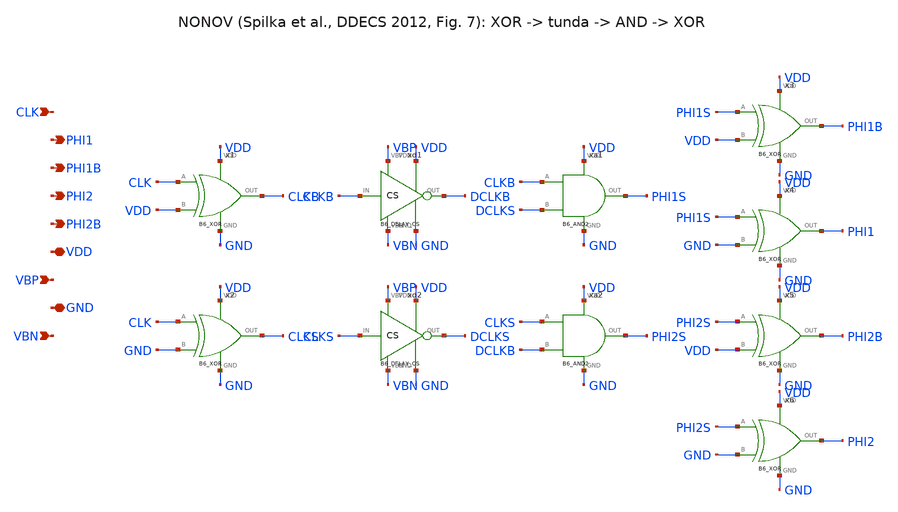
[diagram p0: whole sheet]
** sch_path: blocks/06_Clock_gen/xschem/B6_NONOV.sch
**.subckt B6_NONOV CLK PHI1 PHI1B PHI2 PHI2B VDD VBP GND VBN
*.ipin CLK
*.opin PHI1
*.opin PHI1B
*.opin PHI2
*.opin PHI2B
*.iopin VDD
*.ipin VBP
*.iopin GND
*.ipin VBN
x1 CLK VDD CLKB VDD GND B6_XOR
x2 CLK GND CLKS VDD GND B6_XOR
xd1 CLKB DCLKB VBP VDD VBN GND B6_DELAY_CS
xd2 CLKS DCLKS VBP VDD VBN GND B6_DELAY_CS
xa1 CLKB DCLKS PHI1S VDD GND B6_AND2
xa2 CLKS DCLKB PHI2S VDD GND B6_AND2
x3 PHI1S VDD PHI1B VDD GND B6_XOR
x4 PHI1S GND PHI1 VDD GND B6_XOR
x5 PHI2S VDD PHI2B VDD GND B6_XOR
x6 PHI2S GND PHI2 VDD GND B6_XOR
**.ends

* expanding   symbol:  blocks/06_Clock_gen/xschem/B6_XOR.sym # of pins=5
** sym_path: blocks/06_Clock_gen/xschem/B6_XOR.sym
** sch_path: blocks/06_Clock_gen/xschem/B6_XOR.sch
.subckt B6_XOR A B OUT VDD GND
*.ipin A
*.ipin B
*.opin OUT
*.iopin VDD
*.iopin GND
XMPA VDD A net1 VDD sky130_fd_pr__pfet_01v8 L=0.15 W=4 nf=1 ad='int((1 + 1)/2) * 4 / 1 * 0.29' as='int((1 + 2)/2) * 4 / 1 * 0.29'
+ pd='2*int((1 + 1)/2) * (4 / 1 + 0.29)' ps='2*int((1 + 2)/2) * (4 / 1 + 0.29)' nrd='0.29 / 4 ' nrs='0.29 / 4 '
+ sa=0 sb=0 sd=0 mult=1 m=1
XMPB VDD B net1 VDD sky130_fd_pr__pfet_01v8 L=0.15 W=4 nf=1 ad='int((1 + 1)/2) * 4 / 1 * 0.29' as='int((1 + 2)/2) * 4 / 1 * 0.29'
+ pd='2*int((1 + 1)/2) * (4 / 1 + 0.29)' ps='2*int((1 + 2)/2) * (4 / 1 + 0.29)' nrd='0.29 / 4 ' nrs='0.29 / 4 '
+ sa=0 sb=0 sd=0 mult=1 m=1
XMPC net1 C OUT VDD sky130_fd_pr__pfet_01v8 L=0.15 W=4 nf=1 ad='int((1 + 1)/2) * 4 / 1 * 0.29' as='int((1 + 2)/2) * 4 / 1 * 0.29'
+ pd='2*int((1 + 1)/2) * (4 / 1 + 0.29)' ps='2*int((1 + 2)/2) * (4 / 1 + 0.29)' nrd='0.29 / 4 ' nrs='0.29 / 4 '
+ sa=0 sb=0 sd=0 mult=1 m=1
XMNA OUT A net2 GND sky130_fd_pr__nfet_01v8 L=0.15 W=2 nf=1 ad='int((1 + 1)/2) * 2 / 1 * 0.29' as='int((1 + 2)/2) * 2 / 1 * 0.29'
+ pd='2*int((1 + 1)/2) * (2 / 1 + 0.29)' ps='2*int((1 + 2)/2) * (2 / 1 + 0.29)' nrd='0.29 / 2 ' nrs='0.29 / 2 '
+ sa=0 sb=0 sd=0 mult=1 m=1
XMNB net2 B GND GND sky130_fd_pr__nfet_01v8 L=0.15 W=2 nf=1 ad='int((1 + 1)/2) * 2 / 1 * 0.29' as='int((1 + 2)/2) * 2 / 1 * 0.29'
+ pd='2*int((1 + 1)/2) * (2 / 1 + 0.29)' ps='2*int((1 + 2)/2) * (2 / 1 + 0.29)' nrd='0.29 / 2 ' nrs='0.29 / 2 '
+ sa=0 sb=0 sd=0 mult=1 m=1
XMNC OUT C GND GND sky130_fd_pr__nfet_01v8 L=0.15 W=1 nf=1 ad='int((1 + 1)/2) * 1 / 1 * 0.29' as='int((1 + 2)/2) * 1 / 1 * 0.29'
+ pd='2*int((1 + 1)/2) * (1 / 1 + 0.29)' ps='2*int((1 + 2)/2) * (1 / 1 + 0.29)' nrd='0.29 / 1 ' nrs='0.29 / 1 '
+ sa=0 sb=0 sd=0 mult=1 m=1
xnor A B C VDD GND B6_NOR2
.ends


* expanding   symbol:  blocks/06_Clock_gen/xschem/B6_DELAY_CS.sym # of pins=6
** sym_path: blocks/06_Clock_gen/xschem/B6_DELAY_CS.sym
** sch_path: blocks/06_Clock_gen/xschem/B6_DELAY_CS.sch
.subckt B6_DELAY_CS IN OUT VBP VDD VBN GND
*.ipin IN
*.ipin VBP
*.iopin VDD
*.opin OUT
*.ipin VBN
*.iopin GND
XMPS VDD VBP net1 VDD sky130_fd_pr__pfet_01v8 L=1 W=1 nf=1 ad='int((1 + 1)/2) * 1 / 1 * 0.29' as='int((1 + 2)/2) * 1 / 1 * 0.29'
+ pd='2*int((1 + 1)/2) * (1 / 1 + 0.29)' ps='2*int((1 + 2)/2) * (1 / 1 + 0.29)' nrd='0.29 / 1 ' nrs='0.29 / 1 '
+ sa=0 sb=0 sd=0 mult=1 m=1
XMPI net1 IN OUT VDD sky130_fd_pr__pfet_01v8 L=0.15 W=1 nf=1 ad='int((1 + 1)/2) * 1 / 1 * 0.29' as='int((1 + 2)/2) * 1 / 1 * 0.29'
+ pd='2*int((1 + 1)/2) * (1 / 1 + 0.29)' ps='2*int((1 + 2)/2) * (1 / 1 + 0.29)' nrd='0.29 / 1 ' nrs='0.29 / 1 '
+ sa=0 sb=0 sd=0 mult=1 m=1
XMNI OUT IN net2 GND sky130_fd_pr__nfet_01v8 L=0.15 W=0.5 nf=1 ad='int((1 + 1)/2) * 0.5 / 1 * 0.29' as='int((1 + 2)/2) * 0.5 / 1 * 0.29'
+ pd='2*int((1 + 1)/2) * (0.5 / 1 + 0.29)' ps='2*int((1 + 2)/2) * (0.5 / 1 + 0.29)' nrd='0.29 / 0.5 ' nrs='0.29 / 0.5 '
+ sa=0 sb=0 sd=0 mult=1 m=1
XMNS net2 VBN GND GND sky130_fd_pr__nfet_01v8 L=1 W=0.5 nf=1 ad='int((1 + 1)/2) * 0.5 / 1 * 0.29' as='int((1 + 2)/2) * 0.5 / 1 * 0.29'
+ pd='2*int((1 + 1)/2) * (0.5 / 1 + 0.29)' ps='2*int((1 + 2)/2) * (0.5 / 1 + 0.29)' nrd='0.29 / 0.5 ' nrs='0.29 / 0.5 '
+ sa=0 sb=0 sd=0 mult=1 m=1
XC1 OUT GND sky130_fd_pr__cap_mim_m3_1 W=1 L=1 MF=4 m=4
.ends


* expanding   symbol:  blocks/06_Clock_gen/xschem/B6_AND2.sym # of pins=5
** sym_path: blocks/06_Clock_gen/xschem/B6_AND2.sym
** sch_path: blocks/06_Clock_gen/xschem/B6_AND2.sch
.subckt B6_AND2 A B OUT VDD GND
*.ipin A
*.ipin B
*.opin OUT
*.iopin VDD
*.iopin GND
xnand A B net1 VDD GND B6_NAND2
xinv net1 OUT VDD GND B6_INV
.ends


* expanding   symbol:  blocks/06_Clock_gen/xschem/B6_NOR2.sym # of pins=5
** sym_path: blocks/06_Clock_gen/xschem/B6_NOR2.sym
** sch_path: blocks/06_Clock_gen/xschem/B6_NOR2.sch
.subckt B6_NOR2 A B OUT VDD GND
*.ipin A
*.ipin B
*.opin OUT
*.iopin VDD
*.iopin GND
XMPA VDD A net1 VDD sky130_fd_pr__pfet_01v8 L=0.15 W=4 nf=1 ad='int((1 + 1)/2) * 4 / 1 * 0.29' as='int((1 + 2)/2) * 4 / 1 * 0.29'
+ pd='2*int((1 + 1)/2) * (4 / 1 + 0.29)' ps='2*int((1 + 2)/2) * (4 / 1 + 0.29)' nrd='0.29 / 4 ' nrs='0.29 / 4 '
+ sa=0 sb=0 sd=0 mult=1 m=1
XMPB net1 B OUT VDD sky130_fd_pr__pfet_01v8 L=0.15 W=4 nf=1 ad='int((1 + 1)/2) * 4 / 1 * 0.29' as='int((1 + 2)/2) * 4 / 1 * 0.29'
+ pd='2*int((1 + 1)/2) * (4 / 1 + 0.29)' ps='2*int((1 + 2)/2) * (4 / 1 + 0.29)' nrd='0.29 / 4 ' nrs='0.29 / 4 '
+ sa=0 sb=0 sd=0 mult=1 m=1
XMNA OUT A GND GND sky130_fd_pr__nfet_01v8 L=0.15 W=1 nf=1 ad='int((1 + 1)/2) * 1 / 1 * 0.29' as='int((1 + 2)/2) * 1 / 1 * 0.29'
+ pd='2*int((1 + 1)/2) * (1 / 1 + 0.29)' ps='2*int((1 + 2)/2) * (1 / 1 + 0.29)' nrd='0.29 / 1 ' nrs='0.29 / 1 '
+ sa=0 sb=0 sd=0 mult=1 m=1
XMNB OUT B GND GND sky130_fd_pr__nfet_01v8 L=0.15 W=1 nf=1 ad='int((1 + 1)/2) * 1 / 1 * 0.29' as='int((1 + 2)/2) * 1 / 1 * 0.29'
+ pd='2*int((1 + 1)/2) * (1 / 1 + 0.29)' ps='2*int((1 + 2)/2) * (1 / 1 + 0.29)' nrd='0.29 / 1 ' nrs='0.29 / 1 '
+ sa=0 sb=0 sd=0 mult=1 m=1
.ends


* expanding   symbol:  blocks/06_Clock_gen/xschem/B6_NAND2.sym # of pins=5
** sym_path: blocks/06_Clock_gen/xschem/B6_NAND2.sym
** sch_path: blocks/06_Clock_gen/xschem/B6_NAND2.sch
.subckt B6_NAND2 A B OUT VDD GND
*.ipin A
*.ipin B
*.opin OUT
*.iopin VDD
*.iopin GND
XMPA VDD A OUT VDD sky130_fd_pr__pfet_01v8 L=0.15 W=2 nf=1 ad='int((1 + 1)/2) * 2 / 1 * 0.29' as='int((1 + 2)/2) * 2 / 1 * 0.29'
+ pd='2*int((1 + 1)/2) * (2 / 1 + 0.29)' ps='2*int((1 + 2)/2) * (2 / 1 + 0.29)' nrd='0.29 / 2 ' nrs='0.29 / 2 '
+ sa=0 sb=0 sd=0 mult=1 m=1
XMPB VDD B OUT VDD sky130_fd_pr__pfet_01v8 L=0.15 W=2 nf=1 ad='int((1 + 1)/2) * 2 / 1 * 0.29' as='int((1 + 2)/2) * 2 / 1 * 0.29'
+ pd='2*int((1 + 1)/2) * (2 / 1 + 0.29)' ps='2*int((1 + 2)/2) * (2 / 1 + 0.29)' nrd='0.29 / 2 ' nrs='0.29 / 2 '
+ sa=0 sb=0 sd=0 mult=1 m=1
XMNA OUT A net1 GND sky130_fd_pr__nfet_01v8 L=0.15 W=2 nf=1 ad='int((1 + 1)/2) * 2 / 1 * 0.29' as='int((1 + 2)/2) * 2 / 1 * 0.29'
+ pd='2*int((1 + 1)/2) * (2 / 1 + 0.29)' ps='2*int((1 + 2)/2) * (2 / 1 + 0.29)' nrd='0.29 / 2 ' nrs='0.29 / 2 '
+ sa=0 sb=0 sd=0 mult=1 m=1
XMNB net1 B GND GND sky130_fd_pr__nfet_01v8 L=0.15 W=2 nf=1 ad='int((1 + 1)/2) * 2 / 1 * 0.29' as='int((1 + 2)/2) * 2 / 1 * 0.29'
+ pd='2*int((1 + 1)/2) * (2 / 1 + 0.29)' ps='2*int((1 + 2)/2) * (2 / 1 + 0.29)' nrd='0.29 / 2 ' nrs='0.29 / 2 '
+ sa=0 sb=0 sd=0 mult=1 m=1
.ends


* expanding   symbol:  blocks/06_Clock_gen/xschem/B6_INV.sym # of pins=4
** sym_path: blocks/06_Clock_gen/xschem/B6_INV.sym
** sch_path: blocks/06_Clock_gen/xschem/B6_INV.sch
.subckt B6_INV IN OUT VDD GND
*.ipin IN
*.opin OUT
*.iopin VDD
*.iopin GND
XMP VDD IN OUT VDD sky130_fd_pr__pfet_01v8 L=0.15 W=2 nf=1 ad='int((1 + 1)/2) * 2 / 1 * 0.29' as='int((1 + 2)/2) * 2 / 1 * 0.29'
+ pd='2*int((1 + 1)/2) * (2 / 1 + 0.29)' ps='2*int((1 + 2)/2) * (2 / 1 + 0.29)' nrd='0.29 / 2 ' nrs='0.29 / 2 '
+ sa=0 sb=0 sd=0 mult=1 m=1
XMN OUT IN GND GND sky130_fd_pr__nfet_01v8 L=0.15 W=1 nf=1 ad='int((1 + 1)/2) * 1 / 1 * 0.29' as='int((1 + 2)/2) * 1 / 1 * 0.29'
+ pd='2*int((1 + 1)/2) * (1 / 1 + 0.29)' ps='2*int((1 + 2)/2) * (1 / 1 + 0.29)' nrd='0.29 / 1 ' nrs='0.29 / 1 '
+ sa=0 sb=0 sd=0 mult=1 m=1
.ends

.end
